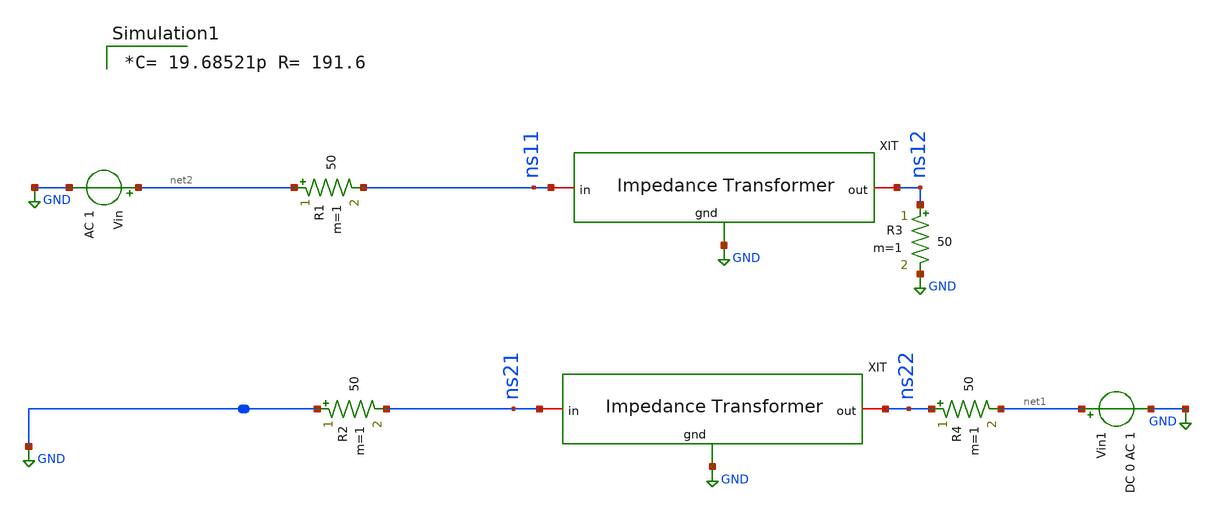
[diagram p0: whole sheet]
** sch_path: impedance-transformer/xschem/impedance-transformer_tb-ac.sch
**.subckt impedance-transformer_tb-ac
Vin1 net1 GND DC 0 AC 1
R3 ns12 GND 50 m=1
R4 ns22 net1 50 m=1
Vin net2 GND AC 1
x1 ns11 ns12 GND impedance-transformer
x2 ns21 ns22 GND impedance-transformer
R1 net2 ns11 50 m=1
R2 GND ns21 50 m=1
**** begin user architecture code



.control
destroy all
save all
ac lin 1MEG 0.1G 3G
set units=degrees
run

set color0=white
set color1=black

let z0=50
let zl=191.7

* Find two S parameters from test circuit
let s11 = v(ns11)
let s12 = v(ns12)
let s21 = v(ns21)
let s22 = v(ns22)

* Extract Y parameters
*let StoYDelS = ((1+s11)*(1+s22)-s12*s21)*z0
*let y11 = ((1+s22)*(1-s11)+s12*s21/StoYDelS
*let y12=-2*s12/StoYDelS
*let y21=-2*s21/StoYDelS
*let y22 = ((1+s11)*(1-s22)+s12+s21)/StoYDelS

* Extract Z parameters
let StoZDelS = ((1-s11)*(1-s22)-s12*s21)/z0
let z11 = ((1+s11)*(1-s22)+s12*s21)/StoZDelS
let z12 = 2*s12/StoZDelS
let z21 = 2*s21/StoZDelS
let z22=((1-s11)*(1+s22)+s12*s21)/StoZDelS

let z_in =z11-z12*z21/(z22+z0)
let z_output=z22-(z12*z21/(z11+z0))
plot ph(z_in) ph(z_output)
plot mag(z_in) mag(z_output)
let gamma=(mag(z_output)-mag(z_in))/(mag(z_output)+mag(z_in))
plot gamma
.endc

 .lib $::SKYWATER_MODELS/sky130.lib.spice tt
.include $::SKYWATER_STDCELLS/sky130_fd_sc_hd.spice


*C= 19.68521p R= 191.6

**** end user architecture code
**.ends

* expanding   symbol:
*+  /home/hugodg/projects-sky130/temp-sensor/impedance-transformer/xschem/impedance-transformer.sym # of pins=3
** sym_path: impedance-transformer/xschem/impedance-transformer.sym
** sch_path: impedance-transformer/xschem/impedance-transformer.sch
.subckt impedance-transformer in out gnd
*.iopin gnd
*.iopin in
*.iopin out
XC0 in gnd sky130_fd_pr__cap_mim_m3_2 W=23.2 L=23.2 MF=25 m=25
XC1 out gnd sky130_fd_pr__cap_mim_m3_2 W=25.2 L=25.2 MF=25 m=25
x1 in out l1
**** begin user architecture code

* NGSPICE file created from impedance-transformer.ext - technology: sky





**** end user architecture code
.ends


* expanding   symbol:  /home/hugodg/projects-sky130/temp-sensor/impedance-transformer/xschem/l1.sym
*+ # of pins=2
** sym_path: impedance-transformer/xschem/l1.sym
** sch_path: impedance-transformer/xschem/l1.sch
.subckt l1 p1 p2
*.iopin p2
*.iopin p1
L0 p1 net3 598p m=1
Cs1 p1 net1 26.59f m=1
Cs2 p2 net2 25.14f m=1
Rs1 net1 GND 63.55 m=1
Rs2 net2 GND 19.11 m=1
R1 p2 net3 2.89 m=1
.ends

.GLOBAL GND
.end
